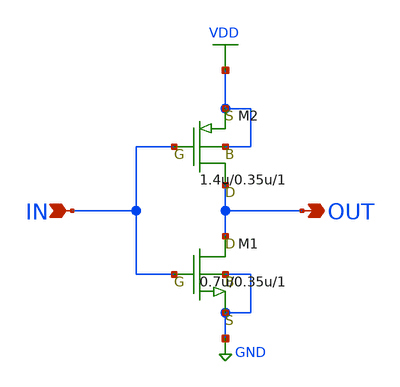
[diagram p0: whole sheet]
** sch_path: LR_hokari/LR_Work2/Clocked_Comparator_Xschem/INVERTER_MIN.sch
**.subckt INVERTER_MIN IN OUT
*.ipin IN
*.opin OUT
M1 OUT IN GND GND nch w=0.7u l=0.35u as=0.56p ps=3u ad=0.56p pd=3u m=1
M2 OUT IN VDD VDD pch w=1.4u l=0.35u as=1.2p ps=4.6u ad=1.2p pd=4.6u m=1
**.ends
.GLOBAL GND
.GLOBAL VDD
.end
